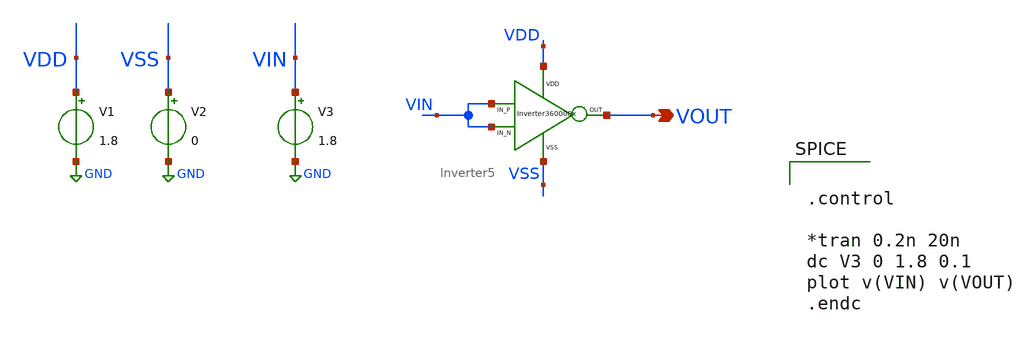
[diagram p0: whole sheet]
** sch_path: xschem/DC_DC_Converter_xschem/OTHERS/DC_DC_Converter_JV10/Inverter_5/Inverter5_TB.sch
**.subckt Inverter5_TB VOUT
*.opin VOUT
V1 VDD GND 1.8
V2 VSS GND 0
V3 VIN GND 1.8
X2 VOUT VDD VSS VIN VIN Inverter5
**** begin user architecture code


.control

*tran 0.2n 20n
dc V3 0 1.8 0.1
plot v(VIN) v(VOUT)
.endc



** opencircuitdesign pdks install
.lib $::SKYWATER_MODELS/sky130.lib.spice tt


**** end user architecture code
**.ends
.GLOBAL GND
.end
